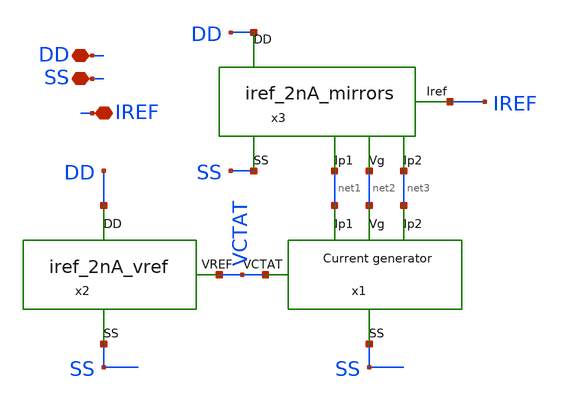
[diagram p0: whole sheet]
** sch_path: xschem/iref_2nA.sch
**.subckt iref_2nA DD SS IREF
*.iopin DD
*.iopin SS
*.iopin IREF
x1 net3 SS net1 VCTAT net2 iref_2nA_igenerator
x3 DD SS net1 net2 net3 IREF iref_2nA_mirrors
x2 VCTAT DD SS iref_2nA_vref
**.ends

* expanding   symbol:  iref_2nA_igenerator.sym # of pins=5
** sym_path: xschem/iref_2nA_igenerator.sym
** sch_path: xschem/iref_2nA_igenerator.sch
.subckt iref_2nA_igenerator Ip2 SS Ip1 VCTAT Vg
*.iopin SS
*.ipin VCTAT
*.iopin Ip1
*.iopin Vg
*.iopin Ip2
XM1 Ip1 Vg VPTAT SS sky130_fd_pr__nfet_01v8_lvt L=1 W=2.5 nf=1 ad='int((nf+1)/2) * W/nf * 0.29' as='int((nf+2)/2) * W/nf * 0.29'
+ pd='2*int((nf+1)/2) * (W/nf + 0.29)' ps='2*int((nf+2)/2) * (W/nf + 0.29)' nrd='0.29 / W' nrs='0.29 / W'
+ sa=0 sb=0 sd=0 mult=2 m=2
XM2 Ip2 Vg SS SS sky130_fd_pr__nfet_01v8_lvt L=1 W=2.5 nf=1 ad='int((nf+1)/2) * W/nf * 0.29' as='int((nf+2)/2) * W/nf * 0.29'
+ pd='2*int((nf+1)/2) * (W/nf + 0.29)' ps='2*int((nf+2)/2) * (W/nf + 0.29)' nrd='0.29 / W' nrs='0.29 / W'
+ sa=0 sb=0 sd=0 mult=2 m=2
XM3 VPTAT VCTAT SS SS sky130_fd_pr__nfet_01v8_lvt L=5 W=1 nf=1 ad='int((nf+1)/2) * W/nf * 0.29' as='int((nf+2)/2) * W/nf * 0.29'
+ pd='2*int((nf+1)/2) * (W/nf + 0.29)' ps='2*int((nf+2)/2) * (W/nf + 0.29)' nrd='0.29 / W' nrs='0.29 / W'
+ sa=0 sb=0 sd=0 mult=1 m=1
XM4 SS SS SS SS sky130_fd_pr__nfet_01v8_lvt L=1 W=2.5 nf=1 ad='int((nf+1)/2) * W/nf * 0.29' as='int((nf+2)/2) * W/nf * 0.29'
+ pd='2*int((nf+1)/2) * (W/nf + 0.29)' ps='2*int((nf+2)/2) * (W/nf + 0.29)' nrd='0.29 / W' nrs='0.29 / W'
+ sa=0 sb=0 sd=0 mult=2 m=2
.ends


* expanding   symbol:  iref_2nA_mirrors.sym # of pins=6
** sym_path: xschem/iref_2nA_mirrors.sym
** sch_path: xschem/iref_2nA_mirrors.sch
.subckt iref_2nA_mirrors DD SS Ip1 Vg Ip2 Iref
*.iopin DD
*.iopin SS
*.iopin Iref
*.iopin Ip2
*.iopin Vg
*.iopin Ip1
XM7 net3 Ip2 DD DD sky130_fd_pr__pfet_01v8_lvt L=2 W=2.5 nf=1 ad='int((nf+1)/2) * W/nf * 0.29' as='int((nf+2)/2) * W/nf * 0.29'
+ pd='2*int((nf+1)/2) * (W/nf + 0.29)' ps='2*int((nf+2)/2) * (W/nf + 0.29)' nrd='0.29 / W' nrs='0.29 / W'
+ sa=0 sb=0 sd=0 mult=10 m=10
XM8 net2 Ip1 DD DD sky130_fd_pr__pfet_01v8_lvt L=2 W=2.5 nf=1 ad='int((nf+1)/2) * W/nf * 0.29' as='int((nf+2)/2) * W/nf * 0.29'
+ pd='2*int((nf+1)/2) * (W/nf + 0.29)' ps='2*int((nf+2)/2) * (W/nf + 0.29)' nrd='0.29 / W' nrs='0.29 / W'
+ sa=0 sb=0 sd=0 mult=2 m=2
XM9 net4 Ip2 DD DD sky130_fd_pr__pfet_01v8_lvt L=2 W=2.5 nf=1 ad='int((nf+1)/2) * W/nf * 0.29' as='int((nf+2)/2) * W/nf * 0.29'
+ pd='2*int((nf+1)/2) * (W/nf + 0.29)' ps='2*int((nf+2)/2) * (W/nf + 0.29)' nrd='0.29 / W' nrs='0.29 / W'
+ sa=0 sb=0 sd=0 mult=2 m=2
XM10 net1 Ip1 DD DD sky130_fd_pr__pfet_01v8_lvt L=2 W=2.5 nf=1 ad='int((nf+1)/2) * W/nf * 0.29' as='int((nf+2)/2) * W/nf * 0.29'
+ pd='2*int((nf+1)/2) * (W/nf + 0.29)' ps='2*int((nf+2)/2) * (W/nf + 0.29)' nrd='0.29 / W' nrs='0.29 / W'
+ sa=0 sb=0 sd=0 mult=2 m=2
XM11 Vn Vn SS SS sky130_fd_pr__nfet_01v8_lvt L=1 W=2.5 nf=1 ad='int((nf+1)/2) * W/nf * 0.29' as='int((nf+2)/2) * W/nf * 0.29'
+ pd='2*int((nf+1)/2) * (W/nf + 0.29)' ps='2*int((nf+2)/2) * (W/nf + 0.29)' nrd='0.29 / W' nrs='0.29 / W'
+ sa=0 sb=0 sd=0 mult=2 m=2
XM12 Vg Vn SS SS sky130_fd_pr__nfet_01v8_lvt L=1 W=2.5 nf=1 ad='int((nf+1)/2) * W/nf * 0.29' as='int((nf+2)/2) * W/nf * 0.29'
+ pd='2*int((nf+1)/2) * (W/nf + 0.29)' ps='2*int((nf+2)/2) * (W/nf + 0.29)' nrd='0.29 / W' nrs='0.29 / W'
+ sa=0 sb=0 sd=0 mult=2 m=2
XM15 net5 Ip2 DD DD sky130_fd_pr__pfet_01v8_lvt L=2 W=2.5 nf=1 ad='int((nf+1)/2) * W/nf * 0.29' as='int((nf+2)/2) * W/nf * 0.29'
+ pd='2*int((nf+1)/2) * (W/nf + 0.29)' ps='2*int((nf+2)/2) * (W/nf + 0.29)' nrd='0.29 / W' nrs='0.29 / W'
+ sa=0 sb=0 sd=0 mult=2 m=2
XM16 Vg Vb net2 DD sky130_fd_pr__pfet_01v8_lvt L=2 W=2.5 nf=1 ad='int((nf+1)/2) * W/nf * 0.29' as='int((nf+2)/2) * W/nf * 0.29'
+ pd='2*int((nf+1)/2) * (W/nf + 0.29)' ps='2*int((nf+2)/2) * (W/nf + 0.29)' nrd='0.29 / W' nrs='0.29 / W'
+ sa=0 sb=0 sd=0 mult=2 m=2
XM17 Ip1 Vb net1 DD sky130_fd_pr__pfet_01v8_lvt L=2 W=2.5 nf=1 ad='int((nf+1)/2) * W/nf * 0.29' as='int((nf+2)/2) * W/nf * 0.29'
+ pd='2*int((nf+1)/2) * (W/nf + 0.29)' ps='2*int((nf+2)/2) * (W/nf + 0.29)' nrd='0.29 / W' nrs='0.29 / W'
+ sa=0 sb=0 sd=0 mult=2 m=2
XM18 Ip2 Vb net3 DD sky130_fd_pr__pfet_01v8_lvt L=2 W=2.5 nf=1 ad='int((nf+1)/2) * W/nf * 0.29' as='int((nf+2)/2) * W/nf * 0.29'
+ pd='2*int((nf+1)/2) * (W/nf + 0.29)' ps='2*int((nf+2)/2) * (W/nf + 0.29)' nrd='0.29 / W' nrs='0.29 / W'
+ sa=0 sb=0 sd=0 mult=10 m=10
XM19 Vn Vb net4 DD sky130_fd_pr__pfet_01v8_lvt L=2 W=2.5 nf=1 ad='int((nf+1)/2) * W/nf * 0.29' as='int((nf+2)/2) * W/nf * 0.29'
+ pd='2*int((nf+1)/2) * (W/nf + 0.29)' ps='2*int((nf+2)/2) * (W/nf + 0.29)' nrd='0.29 / W' nrs='0.29 / W'
+ sa=0 sb=0 sd=0 mult=2 m=2
XM20 Iref Vb net5 DD sky130_fd_pr__pfet_01v8_lvt L=2 W=2.5 nf=1 ad='int((nf+1)/2) * W/nf * 0.29' as='int((nf+2)/2) * W/nf * 0.29'
+ pd='2*int((nf+1)/2) * (W/nf + 0.29)' ps='2*int((nf+2)/2) * (W/nf + 0.29)' nrd='0.29 / W' nrs='0.29 / W'
+ sa=0 sb=0 sd=0 mult=2 m=2
XM22 net6 net6 DD DD sky130_fd_pr__pfet_01v8_lvt L=2 W=2.5 nf=1 ad='int((nf+1)/2) * W/nf * 0.29' as='int((nf+2)/2) * W/nf * 0.29'
+ pd='2*int((nf+1)/2) * (W/nf + 0.29)' ps='2*int((nf+2)/2) * (W/nf + 0.29)' nrd='0.29 / W' nrs='0.29 / W'
+ sa=0 sb=0 sd=0 mult=2 m=2
XM21 Vb Vn SS SS sky130_fd_pr__nfet_01v8_lvt L=1 W=2.5 nf=1 ad='int((nf+1)/2) * W/nf * 0.29' as='int((nf+2)/2) * W/nf * 0.29'
+ pd='2*int((nf+1)/2) * (W/nf + 0.29)' ps='2*int((nf+2)/2) * (W/nf + 0.29)' nrd='0.29 / W' nrs='0.29 / W'
+ sa=0 sb=0 sd=0 mult=2 m=2
XM23 Vb Vb net6 DD sky130_fd_pr__pfet_01v8_lvt L=2 W=2.5 nf=1 ad='int((nf+1)/2) * W/nf * 0.29' as='int((nf+2)/2) * W/nf * 0.29'
+ pd='2*int((nf+1)/2) * (W/nf + 0.29)' ps='2*int((nf+2)/2) * (W/nf + 0.29)' nrd='0.29 / W' nrs='0.29 / W'
+ sa=0 sb=0 sd=0 mult=2 m=2
XM1 DD DD DD DD sky130_fd_pr__pfet_01v8_lvt L=2 W=0.5 nf=1 ad='int((nf+1)/2) * W/nf * 0.29' as='int((nf+2)/2) * W/nf * 0.29'
+ pd='2*int((nf+1)/2) * (W/nf + 0.29)' ps='2*int((nf+2)/2) * (W/nf + 0.29)' nrd='0.29 / W' nrs='0.29 / W'
+ sa=0 sb=0 sd=0 mult=8 m=8
XM2 SS SS SS SS sky130_fd_pr__nfet_01v8_lvt L=1 W=2.5 nf=1 ad='int((nf+1)/2) * W/nf * 0.29' as='int((nf+2)/2) * W/nf * 0.29'
+ pd='2*int((nf+1)/2) * (W/nf + 0.29)' ps='2*int((nf+2)/2) * (W/nf + 0.29)' nrd='0.29 / W' nrs='0.29 / W'
+ sa=0 sb=0 sd=0 mult=2 m=2
.ends


* expanding   symbol:  iref_2nA_vref.sym # of pins=3
** sym_path: xschem/iref_2nA_vref.sym
** sch_path: xschem/iref_2nA_vref.sch
.subckt iref_2nA_vref VREF DD SS
*.iopin DD
*.iopin SS
*.iopin VREF
XM1 N2 N1 DD DD sky130_fd_pr__pfet_01v8 L=4.38 W=2.37 nf=1 ad='int((nf+1)/2) * W/nf * 0.29' as='int((nf+2)/2) * W/nf * 0.29'
+ pd='2*int((nf+1)/2) * (W/nf + 0.29)' ps='2*int((nf+2)/2) * (W/nf + 0.29)' nrd='0.29 / W' nrs='0.29 / W'
+ sa=0 sb=0 sd=0 mult=1 m=1
XM2 SS N2 N2 N2 sky130_fd_pr__pfet_01v8_lvt L=6.97 W=0.88 nf=1 ad='int((nf+1)/2) * W/nf * 0.29' as='int((nf+2)/2) * W/nf * 0.29'
+ pd='2*int((nf+1)/2) * (W/nf + 0.29)' ps='2*int((nf+2)/2) * (W/nf + 0.29)' nrd='0.29 / W' nrs='0.29 / W'
+ sa=0 sb=0 sd=0 mult=1 m=1
XM3 N1 DD DD DD sky130_fd_pr__pfet_01v8_lvt L=4 W=0.5 nf=1 ad='int((nf+1)/2) * W/nf * 0.29' as='int((nf+2)/2) * W/nf * 0.29'
+ pd='2*int((nf+1)/2) * (W/nf + 0.29)' ps='2*int((nf+2)/2) * (W/nf + 0.29)' nrd='0.29 / W' nrs='0.29 / W'
+ sa=0 sb=0 sd=0 mult=1 m=1
XM4 VREF N2 N1 DD sky130_fd_pr__pfet_01v8_lvt L=2.77 W=3.43 nf=1 ad='int((nf+1)/2) * W/nf * 0.29' as='int((nf+2)/2) * W/nf * 0.29'
+ pd='2*int((nf+1)/2) * (W/nf + 0.29)' ps='2*int((nf+2)/2) * (W/nf + 0.29)' nrd='0.29 / W' nrs='0.29 / W'
+ sa=0 sb=0 sd=0 mult=1 m=1
XM5 SS SS VREF VREF sky130_fd_pr__pfet_01v8 L=0.5 W=2 nf=1 ad='int((nf+1)/2) * W/nf * 0.29' as='int((nf+2)/2) * W/nf * 0.29'
+ pd='2*int((nf+1)/2) * (W/nf + 0.29)' ps='2*int((nf+2)/2) * (W/nf + 0.29)' nrd='0.29 / W' nrs='0.29 / W'
+ sa=0 sb=0 sd=0 mult=4 m=4
.ends

.end
